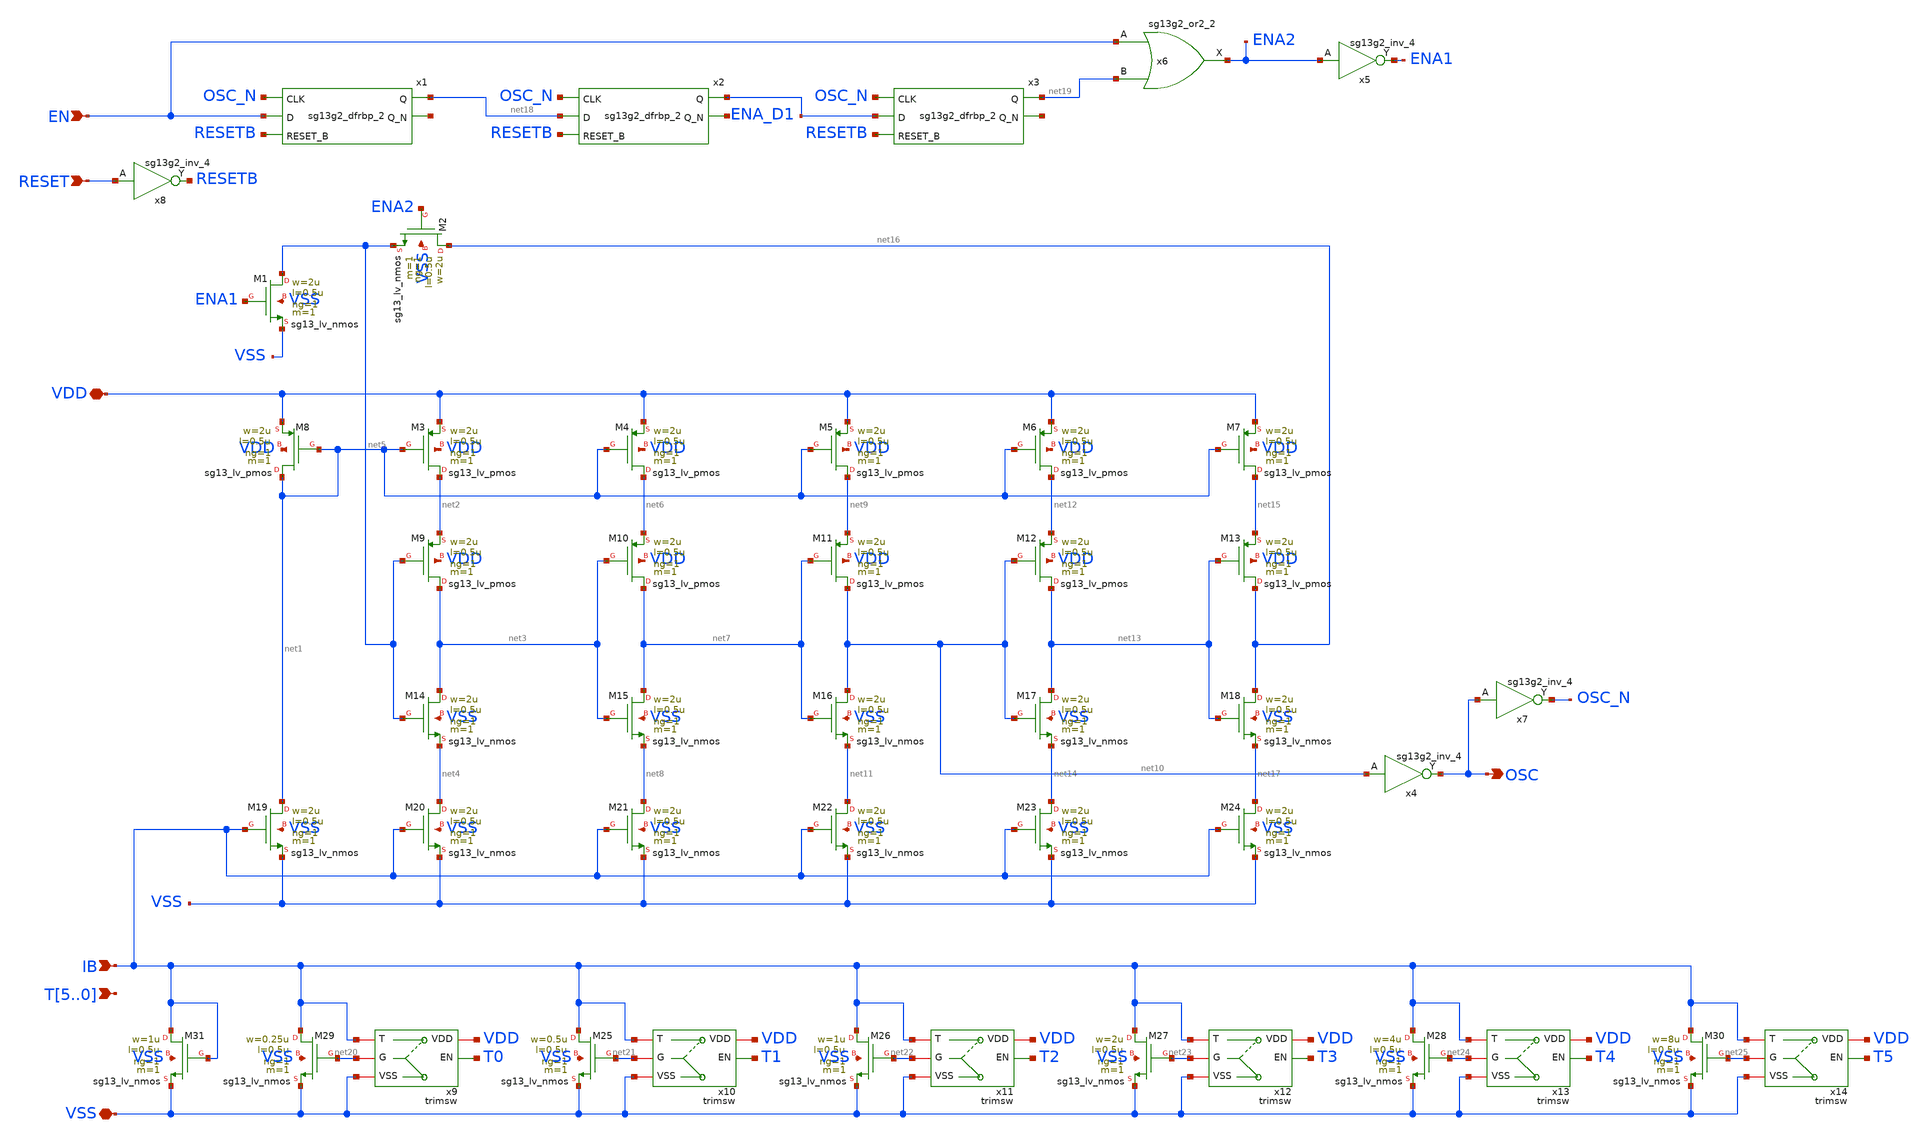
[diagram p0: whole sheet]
** sch_path: ip/riosc/xschem/riosc.sch
* IHP-GmbH/IHP-Open-PDK/ihp-sg13g2/libs.tech/xschem/sg13g2_stdcells/sg13g2_inv_4.sch:
* Copyright 2023 IHP PDK Authors
* Licensed under the Apache License, Version 2.0 (the "License");
**.subckt riosc VSS VDD IB OSC EN RESET T5,T4,T3,T2,T1,T0
*.iopin VSS
*.iopin VDD
*.ipin IB
*.opin OSC
*.ipin EN
*.ipin RESET
*.ipin T5,T4,T3,T2,T1,T0
x8 RESETB RESET VDD VSS sg13g2_inv_4
x5 ENA1 ENA2 VDD VSS sg13g2_inv_4
x6 ENA2 EN net19 VDD VSS sg13g2_or2_2
x1 net18 net26 OSC_N EN RESETB VDD VSS sg13g2_dfrbp_2
x2 ENA_D1 net27 OSC_N net18 RESETB VDD VSS sg13g2_dfrbp_2
x3 net19 net28 OSC_N ENA_D1 RESETB VDD VSS sg13g2_dfrbp_2
x4 OSC net10 VDD VSS sg13g2_inv_4
x7 OSC_N OSC VDD VSS sg13g2_inv_4
XM1 net5 ENA1 VSS VSS sg13_lv_nmos w=2u l=0.5u ng=1 m=1 mm_ok=1
XM2 net16 ENA2 net5 VSS sg13_lv_nmos w=2u l=0.5u ng=1 m=1 mm_ok=1
XM3 net2 net1 VDD VDD sg13_lv_pmos w=2u l=0.5u ng=1 m=1 mm_ok=1
XM4 net6 net1 VDD VDD sg13_lv_pmos w=2u l=0.5u ng=1 m=1 mm_ok=1
XM5 net9 net1 VDD VDD sg13_lv_pmos w=2u l=0.5u ng=1 m=1 mm_ok=1
XM6 net12 net1 VDD VDD sg13_lv_pmos w=2u l=0.5u ng=1 m=1 mm_ok=1
XM7 net15 net1 VDD VDD sg13_lv_pmos w=2u l=0.5u ng=1 m=1 mm_ok=1
XM8 net1 net1 VDD VDD sg13_lv_pmos w=2u l=0.5u ng=1 m=1 mm_ok=1
XM9 net3 net5 net2 VDD sg13_lv_pmos w=2u l=0.5u ng=1 m=1 mm_ok=1
XM10 net7 net3 net6 VDD sg13_lv_pmos w=2u l=0.5u ng=1 m=1 mm_ok=1
XM11 net10 net7 net9 VDD sg13_lv_pmos w=2u l=0.5u ng=1 m=1 mm_ok=1
XM12 net13 net10 net12 VDD sg13_lv_pmos w=2u l=0.5u ng=1 m=1 mm_ok=1
XM13 net16 net13 net15 VDD sg13_lv_pmos w=2u l=0.5u ng=1 m=1 mm_ok=1
XM14 net3 net5 net4 VSS sg13_lv_nmos w=2u l=0.5u ng=1 m=1 mm_ok=1
XM15 net7 net3 net8 VSS sg13_lv_nmos w=2u l=0.5u ng=1 m=1 mm_ok=1
XM16 net10 net7 net11 VSS sg13_lv_nmos w=2u l=0.5u ng=1 m=1 mm_ok=1
XM17 net13 net10 net14 VSS sg13_lv_nmos w=2u l=0.5u ng=1 m=1 mm_ok=1
XM18 net16 net13 net17 VSS sg13_lv_nmos w=2u l=0.5u ng=1 m=1 mm_ok=1
XM19 net1 IB VSS VSS sg13_lv_nmos w=2u l=0.5u ng=1 m=1 mm_ok=1
XM20 net4 IB VSS VSS sg13_lv_nmos w=2u l=0.5u ng=1 m=1 mm_ok=1
XM21 net8 IB VSS VSS sg13_lv_nmos w=2u l=0.5u ng=1 m=1 mm_ok=1
XM22 net11 IB VSS VSS sg13_lv_nmos w=2u l=0.5u ng=1 m=1 mm_ok=1
XM23 net14 IB VSS VSS sg13_lv_nmos w=2u l=0.5u ng=1 m=1 mm_ok=1
XM24 net17 IB VSS VSS sg13_lv_nmos w=2u l=0.5u ng=1 m=1 mm_ok=1
XM29 IB net20 VSS VSS sg13_lv_nmos w=0.25u l=0.5u ng=1 m=1 mm_ok=1
XM31 IB IB VSS VSS sg13_lv_nmos w=1u l=0.5u ng=1 m=1 mm_ok=1
x9 VDD IB T0 net20 VSS trimsw
XM25 IB net21 VSS VSS sg13_lv_nmos w=0.5u l=0.5u ng=1 m=1 mm_ok=1
x10 VDD IB T1 net21 VSS trimsw
XM26 IB net22 VSS VSS sg13_lv_nmos w=1u l=0.5u ng=1 m=1 mm_ok=1
x11 VDD IB T2 net22 VSS trimsw
XM27 IB net23 VSS VSS sg13_lv_nmos w=2u l=0.5u ng=1 m=1 mm_ok=1
x12 VDD IB T3 net23 VSS trimsw
XM28 IB net24 VSS VSS sg13_lv_nmos w=4u l=0.5u ng=1 m=1 mm_ok=1
x13 VDD IB T4 net24 VSS trimsw
XM30 IB net25 VSS VSS sg13_lv_nmos w=8u l=0.5u ng=1 m=1 mm_ok=1
x14 VDD IB T5 net25 VSS trimsw
**** begin user architecture code

.include ${::IHP_STDCELLS}/sg13g2_stdcell.spice

**** end user architecture code
**.ends

* expanding   symbol:  sg13g2_stdcells/sg13g2_inv_4.sym # of pins=2
** sym_path: sg13g2_stdcells/sg13g2_inv_4.sym
** sch_path: sg13g2_stdcells/sg13g2_inv_4.sch
.subckt sg13g2_inv_4 Y A VDD VSS
*.ipin A
*.opin Y
*.iopin VDD
*.iopin VSS
XM1 Y A VSS VSS sg13_lv_nmos w=2.96u l=130.00n ng=4 m=1 mm_ok=1
XM2 Y A VDD VDD sg13_lv_pmos w=4.48u l=130.00n ng=4 m=1 mm_ok=1
.ends


* expanding   symbol:  sg13g2_stdcells/sg13g2_or2_2.sym # of pins=3
** sym_path: sg13g2_stdcells/sg13g2_or2_2.sym
** sch_path: sg13g2_stdcells/sg13g2_or2_2.sch
.subckt sg13g2_or2_2 X A B VDD VSS
*.opin X
*.ipin B
*.ipin A
*.iopin VDD
*.iopin VSS
XM1 net1 B VSS VSS sg13_lv_nmos w=550.00n l=130.00n ng=1 m=1 mm_ok=1
XM2 net1 A VSS VSS sg13_lv_nmos w=550.00n l=130.00n ng=1 m=1 mm_ok=1
XM3 X net1 VSS VSS sg13_lv_nmos w=1.48u l=130.00n ng=2 m=1 mm_ok=1
XM4 net2 A VDD VDD sg13_lv_pmos w=840.00n l=130.00n ng=1 m=1 mm_ok=1
XM5 net1 B net2 VDD sg13_lv_pmos w=840.00n l=130.00n ng=1 m=1 mm_ok=1
XM6 X net1 VDD VDD sg13_lv_pmos w=2.24u l=130.00n ng=2 m=1 mm_ok=1
.ends


* expanding   symbol:  sg13g2_stdcells/sg13g2_dfrbp_2.sym # of pins=5
** sym_path: sg13g2_stdcells/sg13g2_dfrbp_2.sym
** sch_path: sg13g2_stdcells/sg13g2_dfrbp_2.sch
.subckt sg13g2_dfrbp_2 Q Q_N CLK D RESET_B VDD VSS
*.ipin D
*.ipin RESET_B
*.ipin CLK
*.opin Q
*.opin Q_N
*.iopin VDD
*.iopin VSS
XM1 Db D net12 VSS sg13_lv_nmos w=420.00n l=130.00n ng=1 m=1 mm_ok=1
XM2 net12 RESET_B VSS VSS sg13_lv_nmos w=420.00n l=130.00n ng=1 m=1 mm_ok=1
XM3 net2 clkneg net11 VSS sg13_lv_nmos w=420.00n l=130.00n ng=1 m=1 mm_ok=1
XM4 net11 net3 VSS VSS sg13_lv_nmos w=420.00n l=130.00n ng=1 m=1 mm_ok=1
XM5 net3 net2 net7 VSS sg13_lv_nmos w=420.00n l=130.00n ng=1 m=1 mm_ok=1
XM6 net7 RESET_B VSS VSS sg13_lv_nmos w=420.00n l=130.00n ng=1 m=1 mm_ok=1
XM7 Q_N net2 VSS VSS sg13_lv_nmos w=1.48u l=130.00n ng=2 m=1 mm_ok=1
XM8 net1 net2 VSS VSS sg13_lv_nmos w=640.00n l=130.00n ng=1 m=1 mm_ok=1
XM9 Q net1 VSS VSS sg13_lv_nmos w=1.48u l=130.00n ng=2 m=1 mm_ok=1
XM10 clkneg CLK VSS VSS sg13_lv_nmos w=740.00n l=130.00n ng=1 m=1 mm_ok=1
XM11 clkpos clkneg VSS VSS sg13_lv_nmos w=740.00n l=130.00n ng=1 m=1 mm_ok=1
XM12 Db clkneg net4 VSS sg13_lv_nmos w=420.00n l=130.00n ng=1 m=1 mm_ok=1
XM13 net4 clkpos net10 VSS sg13_lv_nmos w=420.00n l=130.00n ng=1 m=1 mm_ok=1
XM14 net10 net5 net6 VSS sg13_lv_nmos w=420.00n l=130.00n ng=1 m=1 mm_ok=1
XM15 net6 RESET_B VSS VSS sg13_lv_nmos w=420.00n l=130.00n ng=1 m=1 mm_ok=1
XM16 net5 net4 VSS VSS sg13_lv_nmos w=740.00n l=130.00n ng=1 m=1 mm_ok=1
XM17 net5 clkpos net2 VSS sg13_lv_nmos w=740.00n l=130.00n ng=1 m=1 mm_ok=1
XM18 Db RESET_B VDD VDD sg13_lv_pmos w=420.00n l=130.00n ng=1 m=1 mm_ok=1
XM19 Db D VDD VDD sg13_lv_pmos w=420.00n l=130.00n ng=1 m=1 mm_ok=1
XM20 net9 net3 VDD VDD sg13_lv_pmos w=420.00n l=130.00n ng=1 m=1 mm_ok=1
XM21 net2 clkpos net9 VDD sg13_lv_pmos w=420.00n l=130.00n ng=1 m=1 mm_ok=1
XM22 net3 net2 VDD VDD sg13_lv_pmos w=420.00n l=130.00n ng=1 m=1 mm_ok=1
XM23 net3 RESET_B VDD VDD sg13_lv_pmos w=420.00n l=130.00n ng=1 m=1 mm_ok=1
XM24 Q_N net2 VDD VDD sg13_lv_pmos w=2.24u l=130.00n ng=2 m=1 mm_ok=1
XM25 net1 net2 VDD VDD sg13_lv_pmos w=1.000u l=130.00n ng=1 m=1 mm_ok=1
XM26 Q net1 VDD VDD sg13_lv_pmos w=2.24u l=130.00n ng=2 m=1 mm_ok=1
XM27 clkneg CLK VDD VDD sg13_lv_pmos w=1.12u l=130.00n ng=1 m=1 mm_ok=1
XM28 clkpos clkneg VDD VDD sg13_lv_pmos w=1.12u l=130.00n ng=1 m=1 mm_ok=1
XM29 Db clkpos net4 VDD sg13_lv_pmos w=420.00n l=130.00n ng=1 m=1 mm_ok=1
XM30 net8 net5 VDD VDD sg13_lv_pmos w=420.00n l=130.00n ng=1 m=1 mm_ok=1
XM31 net4 clkneg net8 VDD sg13_lv_pmos w=420.00n l=130.00n ng=1 m=1 mm_ok=1
XM32 net4 RESET_B VDD VDD sg13_lv_pmos w=420.00n l=130.00n ng=1 m=1 mm_ok=1
XM33 net5 net4 VDD VDD sg13_lv_pmos w=1.000u l=130.00n ng=1 m=1 mm_ok=1
XM34 net5 clkneg net2 VDD sg13_lv_pmos w=1.000u l=130.00n ng=1 m=1 mm_ok=1
.ends


* expanding   symbol:  trimsw.sym # of pins=5
** sym_path: ip/riosc/xschem/trimsw.sym
** sch_path: ip/riosc/xschem/trimsw.sch
.subckt trimsw VDD T EN G VSS
*.iopin G
*.iopin VSS
*.iopin T
*.ipin EN
*.iopin VDD
XM1 G net1 VSS VSS sg13_lv_nmos w=0.5u l=0.25u ng=1 m=1 mm_ok=1
XM2 T net2 G VSS sg13_lv_nmos w=0.5u l=0.25u ng=1 m=1 mm_ok=1
x1 net1 EN VDD VSS sg13g2_not_1
x2 net2 net1 VDD VSS sg13g2_not_1
.ends

.end
